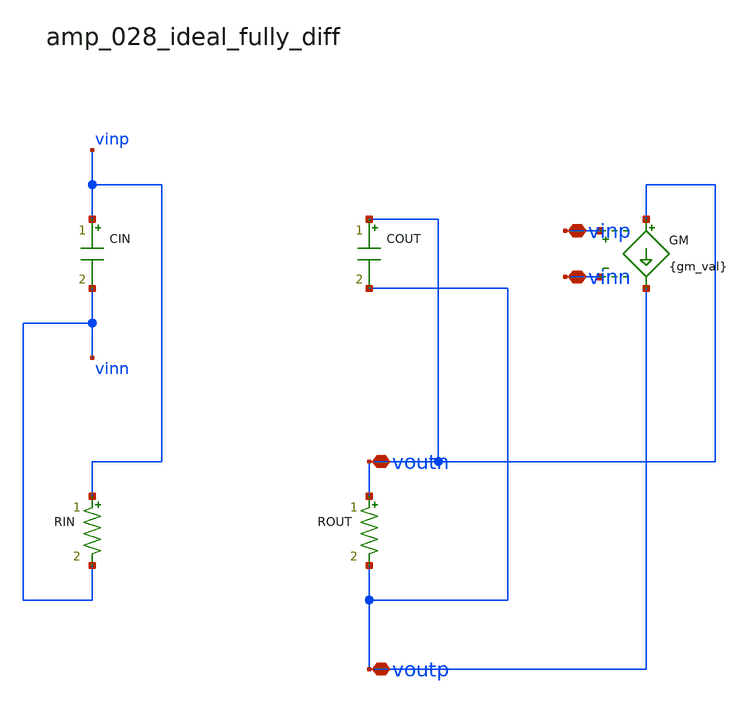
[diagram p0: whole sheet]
** sch_path: analog-db/raw/amp_028_ideal_fully_diff/amp_028_ideal_fully_diff_annotated.sch
**.subckt amp_028_ideal_fully_diff_annotated vinp voutn vinn voutp
*.iopin vinp
*.iopin voutn
*.iopin vinn
*.iopin voutp
CIN vinp vinn 'cin_val' m=1
COUT voutn voutp 'cout_val' m=1
GM voutn voutp vinp vinn {gm_val}
RIN vinp vinn 'rin_val' m=1
ROUT voutn voutp 'rout_val' m=1
**.ends
.end
